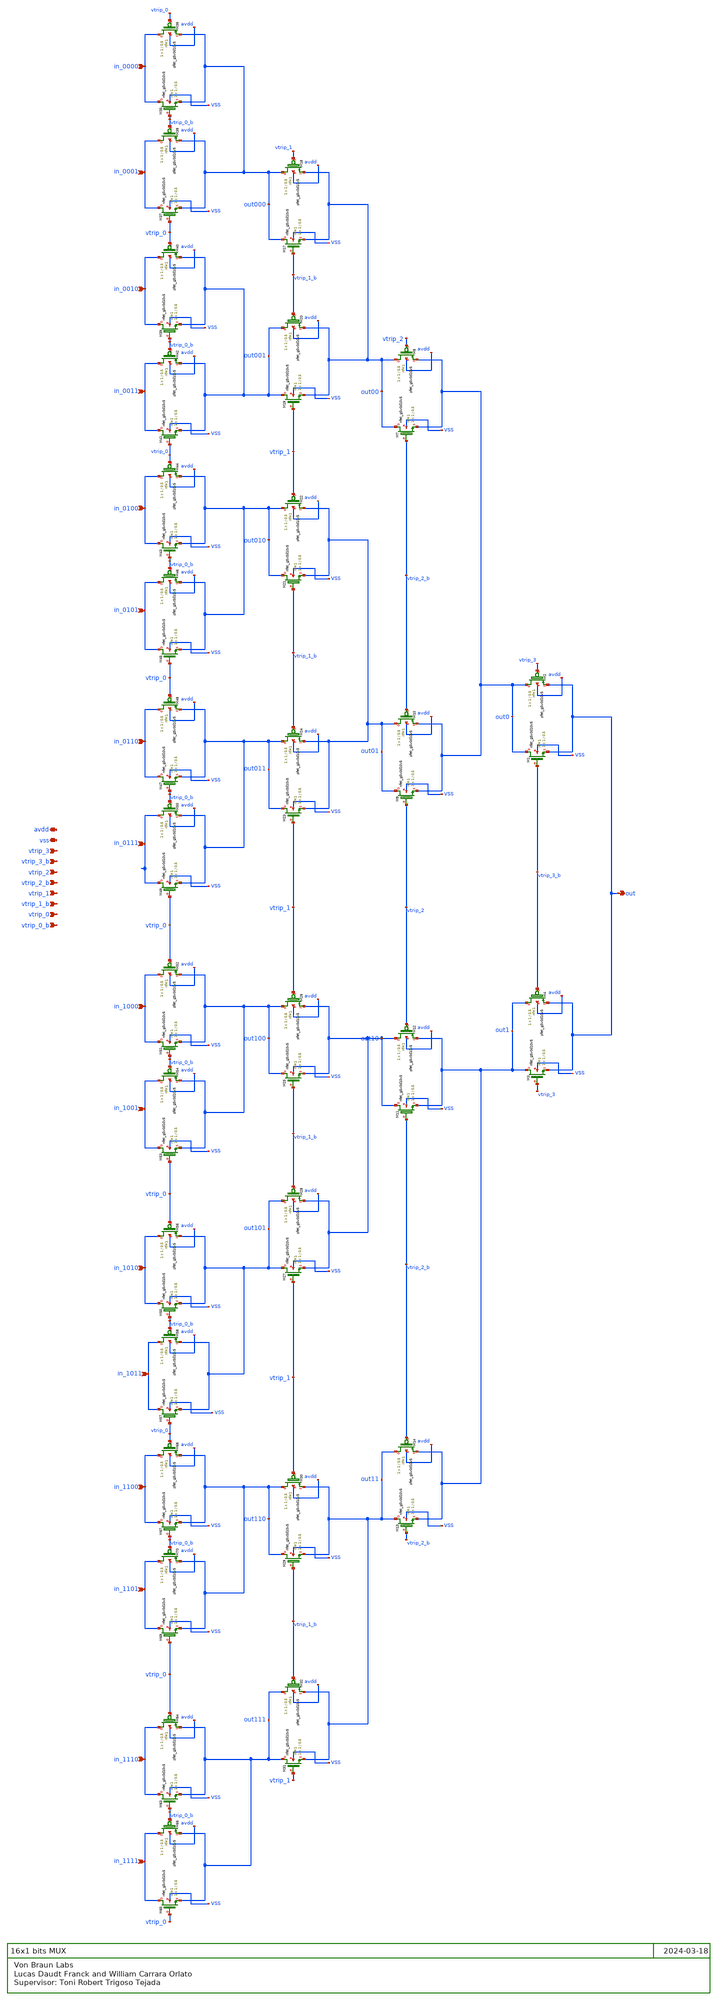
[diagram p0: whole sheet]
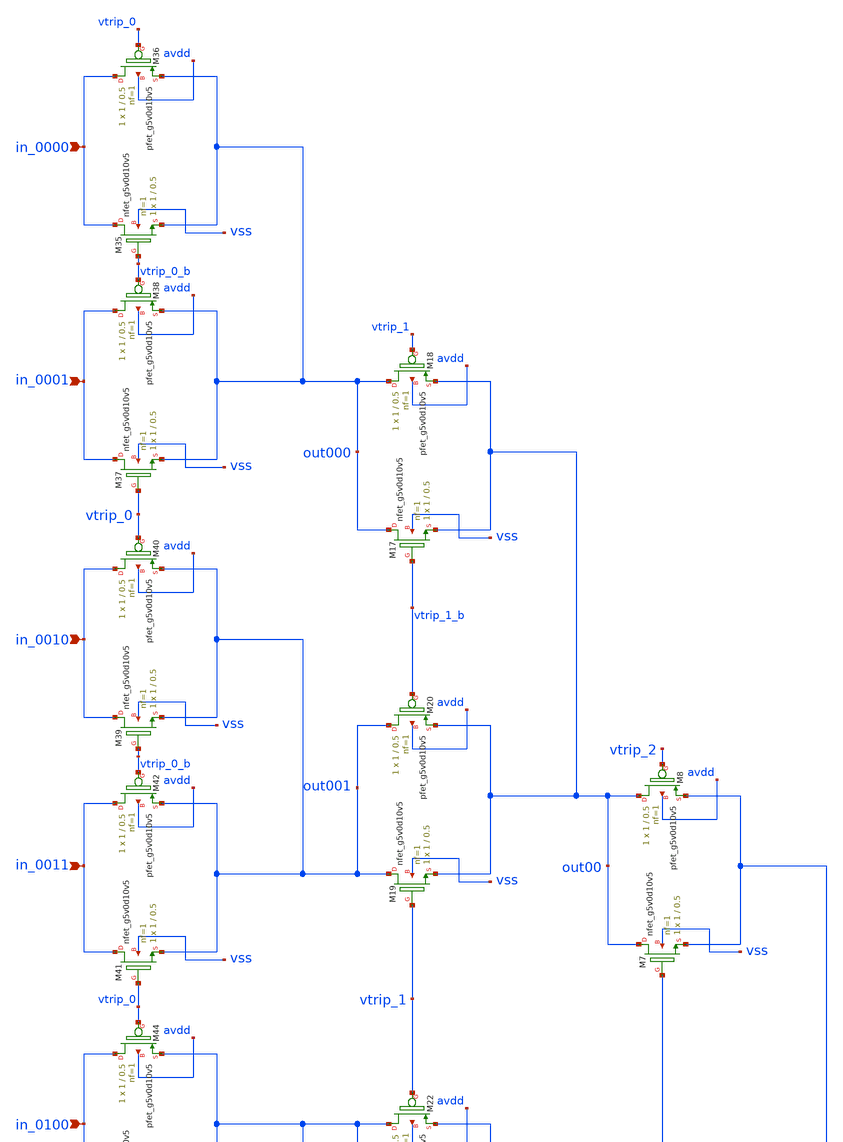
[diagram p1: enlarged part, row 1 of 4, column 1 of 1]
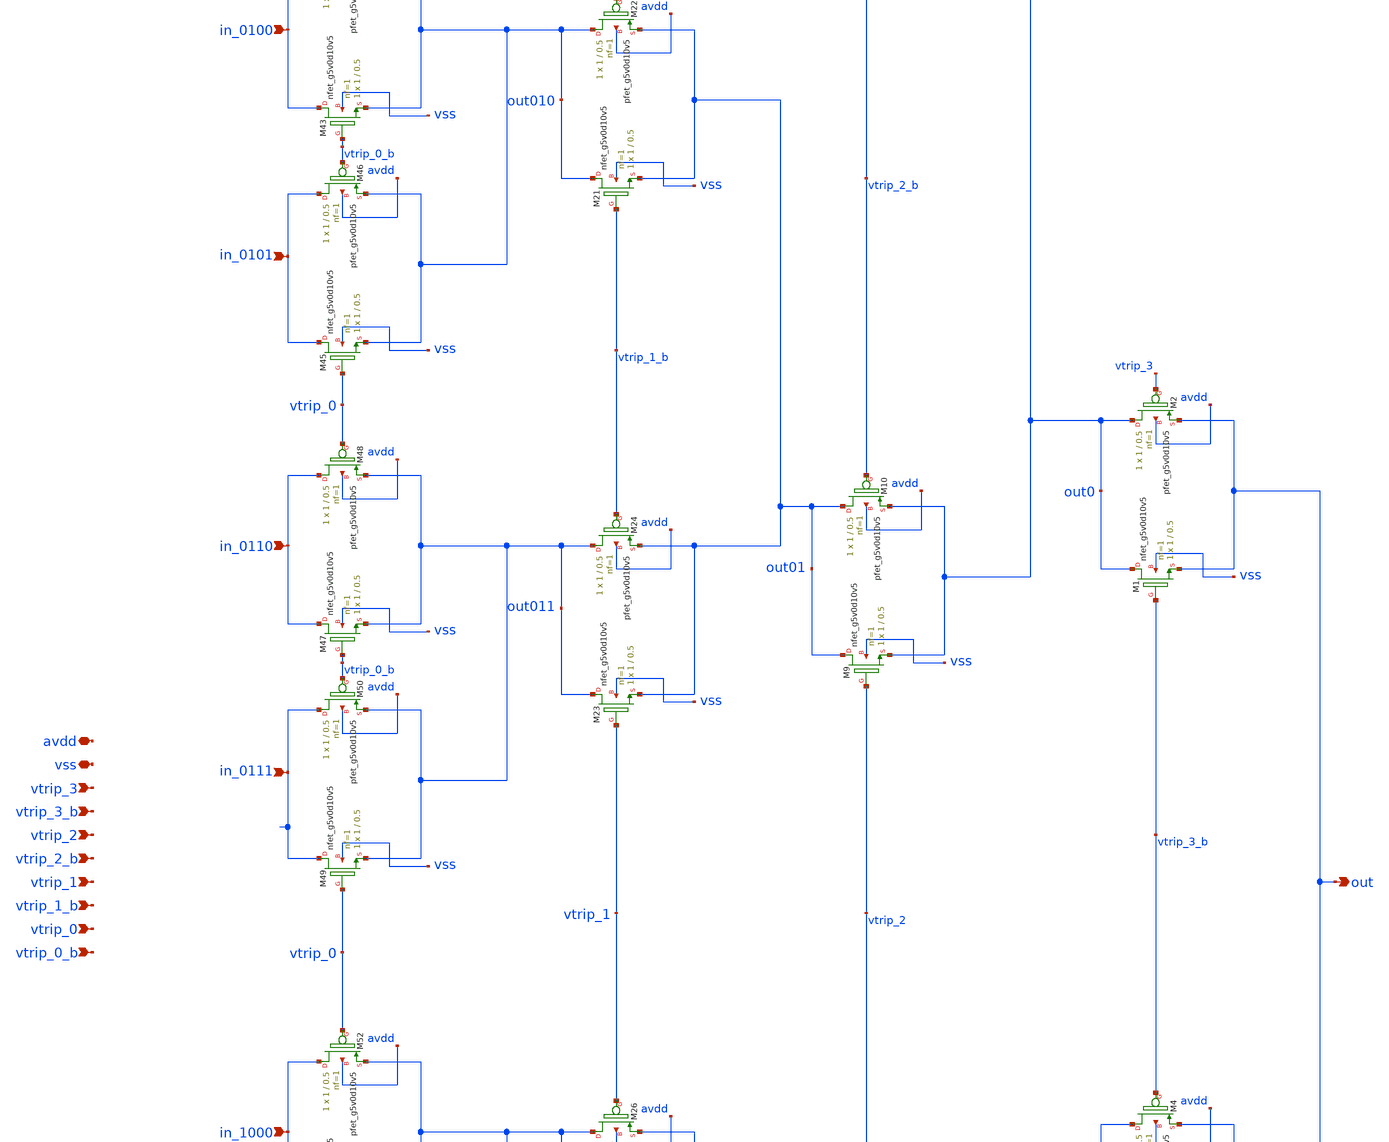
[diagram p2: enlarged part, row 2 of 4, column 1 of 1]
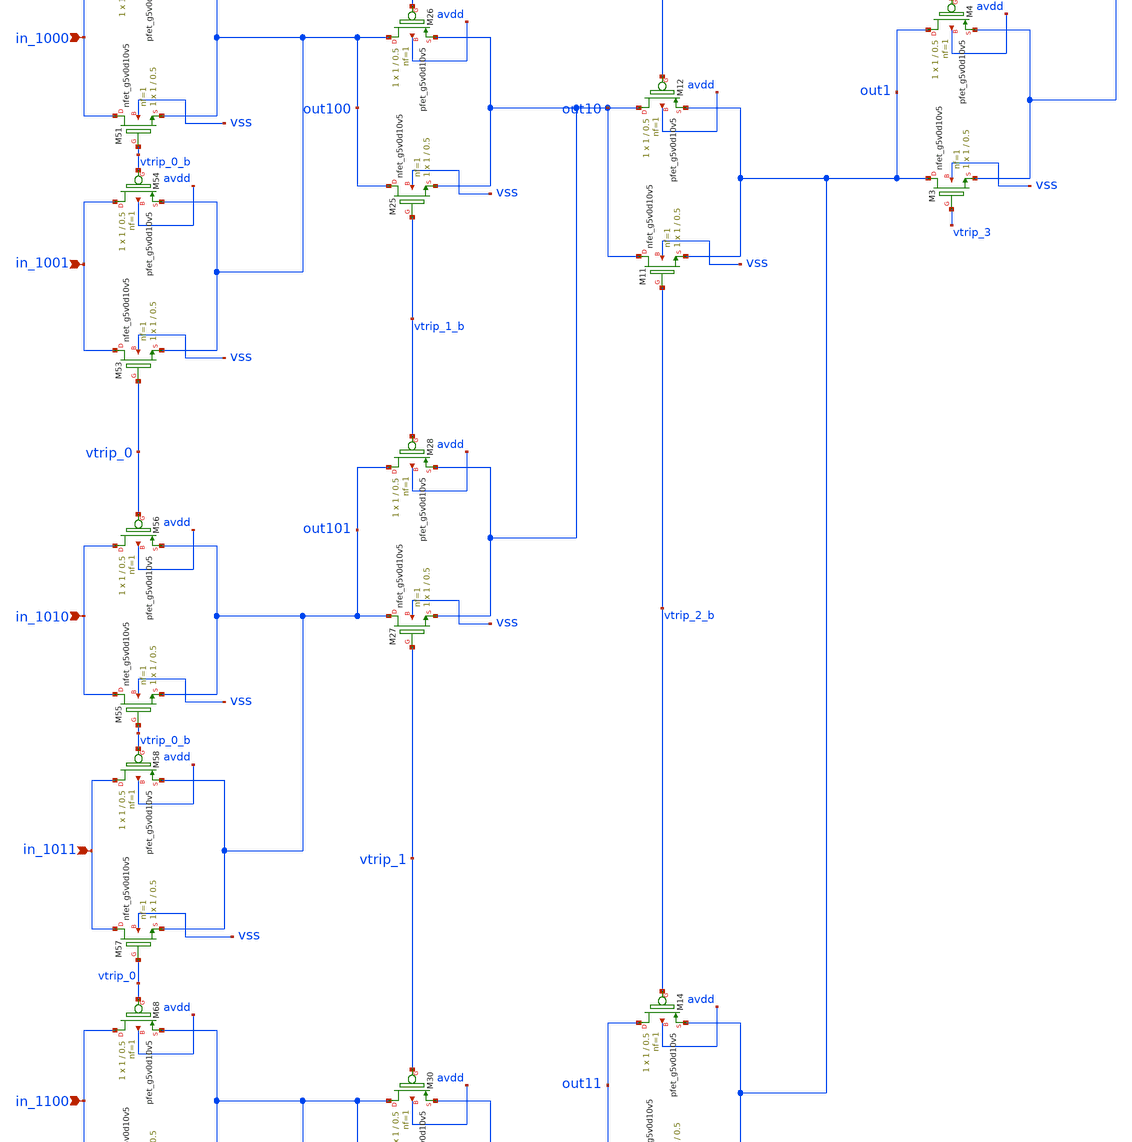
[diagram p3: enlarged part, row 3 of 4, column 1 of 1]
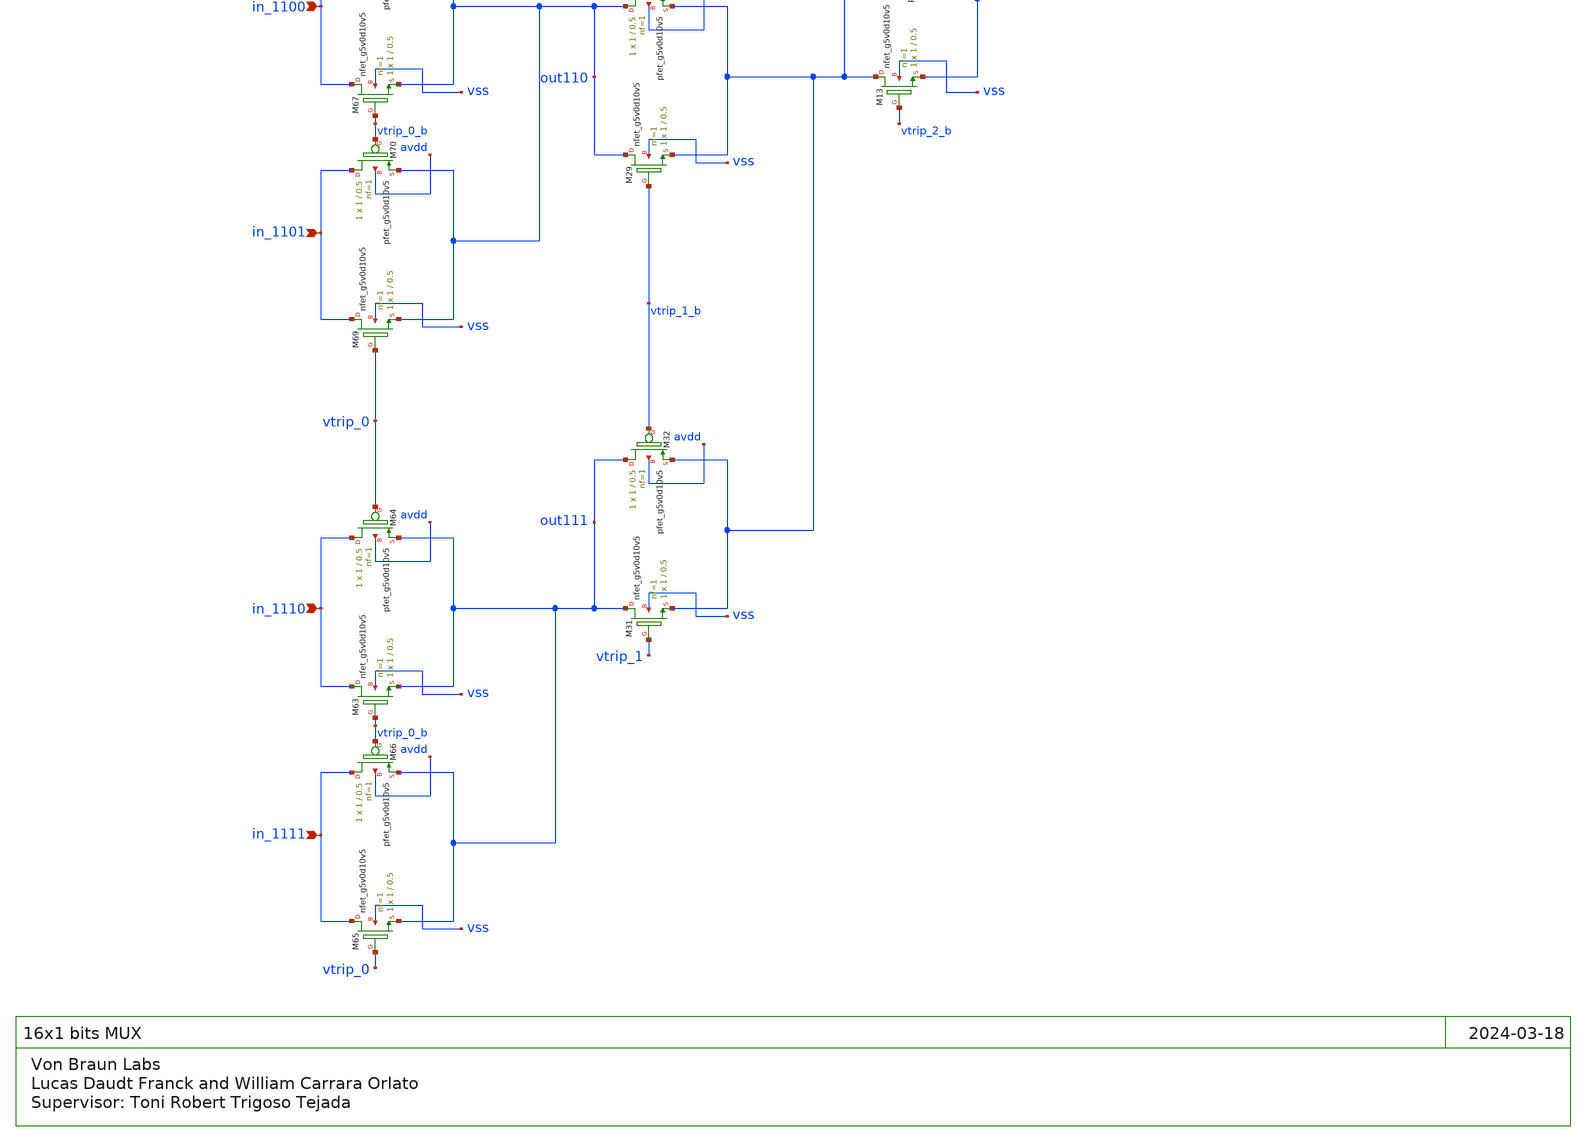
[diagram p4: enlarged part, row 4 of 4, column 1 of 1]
** sch_path: xschem_final/DemuxCompleto.sch
**.subckt DemuxCompleto in_0000 in_0001 in_0010 in_0011 in_0100 in_0101 in_0110 in_0111 in_1000
*+ in_1001 in_1010 in_1011 in_1110 in_1111 in_1100 in_1101 out vtrip_3 vtrip_3_b vtrip_2 vtrip_2_b vtrip_1
*+ vtrip_1_b vtrip_0 vtrip_0_b avdd vss
*.ipin in_0000
*.ipin in_0001
*.ipin in_0010
*.ipin in_0011
*.ipin in_0100
*.ipin in_0101
*.ipin in_0110
*.ipin in_0111
*.ipin in_1000
*.ipin in_1001
*.ipin in_1010
*.ipin in_1011
*.ipin in_1110
*.ipin in_1111
*.ipin in_1100
*.ipin in_1101
*.opin out
*.ipin vtrip_3
*.ipin vtrip_3_b
*.ipin vtrip_2
*.ipin vtrip_2_b
*.ipin vtrip_1
*.ipin vtrip_1_b
*.ipin vtrip_0
*.ipin vtrip_0_b
*.iopin avdd
*.iopin vss
XM1 out0 vtrip_3_b out vss sky130_fd_pr__nfet_g5v0d10v5 L=0.5 W=1 nf=1 ad='int((nf+1)/2) * W/nf * 0.29'
+ as='int((nf+2)/2) * W/nf * 0.29' pd='2*int((nf+1)/2) * (W/nf + 0.29)' ps='2*int((nf+2)/2) * (W/nf + 0.29)'
+ nrd='0.29 / W' nrs='0.29 / W' sa=0 sb=0 sd=0 mult=1 m=1
XM2 out0 vtrip_3 out avdd sky130_fd_pr__pfet_g5v0d10v5 L=0.5 W=1 nf=1 ad='int((nf+1)/2) * W/nf * 0.29'
+ as='int((nf+2)/2) * W/nf * 0.29' pd='2*int((nf+1)/2) * (W/nf + 0.29)' ps='2*int((nf+2)/2) * (W/nf + 0.29)'
+ nrd='0.29 / W' nrs='0.29 / W' sa=0 sb=0 sd=0 mult=1 m=1
XM3 out1 vtrip_3 out vss sky130_fd_pr__nfet_g5v0d10v5 L=0.5 W=1 nf=1 ad='int((nf+1)/2) * W/nf * 0.29'
+ as='int((nf+2)/2) * W/nf * 0.29' pd='2*int((nf+1)/2) * (W/nf + 0.29)' ps='2*int((nf+2)/2) * (W/nf + 0.29)'
+ nrd='0.29 / W' nrs='0.29 / W' sa=0 sb=0 sd=0 mult=1 m=1
XM4 out1 vtrip_3_b out avdd sky130_fd_pr__pfet_g5v0d10v5 L=0.5 W=1 nf=1 ad='int((nf+1)/2) * W/nf * 0.29'
+ as='int((nf+2)/2) * W/nf * 0.29' pd='2*int((nf+1)/2) * (W/nf + 0.29)' ps='2*int((nf+2)/2) * (W/nf + 0.29)'
+ nrd='0.29 / W' nrs='0.29 / W' sa=0 sb=0 sd=0 mult=1 m=1
XM7 out00 vtrip_2_b out0 vss sky130_fd_pr__nfet_g5v0d10v5 L=0.5 W=1 nf=1 ad='int((nf+1)/2) * W/nf * 0.29'
+ as='int((nf+2)/2) * W/nf * 0.29' pd='2*int((nf+1)/2) * (W/nf + 0.29)' ps='2*int((nf+2)/2) * (W/nf + 0.29)'
+ nrd='0.29 / W' nrs='0.29 / W' sa=0 sb=0 sd=0 mult=1 m=1
XM8 out00 vtrip_2 out0 avdd sky130_fd_pr__pfet_g5v0d10v5 L=0.5 W=1 nf=1 ad='int((nf+1)/2) * W/nf * 0.29'
+ as='int((nf+2)/2) * W/nf * 0.29' pd='2*int((nf+1)/2) * (W/nf + 0.29)' ps='2*int((nf+2)/2) * (W/nf + 0.29)'
+ nrd='0.29 / W' nrs='0.29 / W' sa=0 sb=0 sd=0 mult=1 m=1
XM9 out01 vtrip_2 out0 vss sky130_fd_pr__nfet_g5v0d10v5 L=0.5 W=1 nf=1 ad='int((nf+1)/2) * W/nf * 0.29'
+ as='int((nf+2)/2) * W/nf * 0.29' pd='2*int((nf+1)/2) * (W/nf + 0.29)' ps='2*int((nf+2)/2) * (W/nf + 0.29)'
+ nrd='0.29 / W' nrs='0.29 / W' sa=0 sb=0 sd=0 mult=1 m=1
XM10 out01 vtrip_2_b out0 avdd sky130_fd_pr__pfet_g5v0d10v5 L=0.5 W=1 nf=1 ad='int((nf+1)/2) * W/nf * 0.29'
+ as='int((nf+2)/2) * W/nf * 0.29' pd='2*int((nf+1)/2) * (W/nf + 0.29)' ps='2*int((nf+2)/2) * (W/nf + 0.29)'
+ nrd='0.29 / W' nrs='0.29 / W' sa=0 sb=0 sd=0 mult=1 m=1
XM11 out10 vtrip_2_b out1 vss sky130_fd_pr__nfet_g5v0d10v5 L=0.5 W=1 nf=1 ad='int((nf+1)/2) * W/nf * 0.29'
+ as='int((nf+2)/2) * W/nf * 0.29' pd='2*int((nf+1)/2) * (W/nf + 0.29)' ps='2*int((nf+2)/2) * (W/nf + 0.29)'
+ nrd='0.29 / W' nrs='0.29 / W' sa=0 sb=0 sd=0 mult=1 m=1
XM12 out10 vtrip_2 out1 avdd sky130_fd_pr__pfet_g5v0d10v5 L=0.5 W=1 nf=1 ad='int((nf+1)/2) * W/nf * 0.29'
+ as='int((nf+2)/2) * W/nf * 0.29' pd='2*int((nf+1)/2) * (W/nf + 0.29)' ps='2*int((nf+2)/2) * (W/nf + 0.29)'
+ nrd='0.29 / W' nrs='0.29 / W' sa=0 sb=0 sd=0 mult=1 m=1
XM13 out11 vtrip_2_b out1 vss sky130_fd_pr__nfet_g5v0d10v5 L=0.5 W=1 nf=1 ad='int((nf+1)/2) * W/nf * 0.29'
+ as='int((nf+2)/2) * W/nf * 0.29' pd='2*int((nf+1)/2) * (W/nf + 0.29)' ps='2*int((nf+2)/2) * (W/nf + 0.29)'
+ nrd='0.29 / W' nrs='0.29 / W' sa=0 sb=0 sd=0 mult=1 m=1
XM14 out11 vtrip_2_b out1 avdd sky130_fd_pr__pfet_g5v0d10v5 L=0.5 W=1 nf=1 ad='int((nf+1)/2) * W/nf * 0.29'
+ as='int((nf+2)/2) * W/nf * 0.29' pd='2*int((nf+1)/2) * (W/nf + 0.29)' ps='2*int((nf+2)/2) * (W/nf + 0.29)'
+ nrd='0.29 / W' nrs='0.29 / W' sa=0 sb=0 sd=0 mult=1 m=1
XM17 out000 vtrip_1_b out00 vss sky130_fd_pr__nfet_g5v0d10v5 L=0.5 W=1 nf=1 ad='int((nf+1)/2) * W/nf * 0.29'
+ as='int((nf+2)/2) * W/nf * 0.29' pd='2*int((nf+1)/2) * (W/nf + 0.29)' ps='2*int((nf+2)/2) * (W/nf + 0.29)'
+ nrd='0.29 / W' nrs='0.29 / W' sa=0 sb=0 sd=0 mult=1 m=1
XM18 out000 vtrip_1 out00 avdd sky130_fd_pr__pfet_g5v0d10v5 L=0.5 W=1 nf=1 ad='int((nf+1)/2) * W/nf * 0.29'
+ as='int((nf+2)/2) * W/nf * 0.29' pd='2*int((nf+1)/2) * (W/nf + 0.29)' ps='2*int((nf+2)/2) * (W/nf + 0.29)'
+ nrd='0.29 / W' nrs='0.29 / W' sa=0 sb=0 sd=0 mult=1 m=1
XM19 out001 vtrip_1 out00 vss sky130_fd_pr__nfet_g5v0d10v5 L=0.5 W=1 nf=1 ad='int((nf+1)/2) * W/nf * 0.29'
+ as='int((nf+2)/2) * W/nf * 0.29' pd='2*int((nf+1)/2) * (W/nf + 0.29)' ps='2*int((nf+2)/2) * (W/nf + 0.29)'
+ nrd='0.29 / W' nrs='0.29 / W' sa=0 sb=0 sd=0 mult=1 m=1
XM20 out001 vtrip_1_b out00 avdd sky130_fd_pr__pfet_g5v0d10v5 L=0.5 W=1 nf=1 ad='int((nf+1)/2) * W/nf * 0.29'
+ as='int((nf+2)/2) * W/nf * 0.29' pd='2*int((nf+1)/2) * (W/nf + 0.29)' ps='2*int((nf+2)/2) * (W/nf + 0.29)'
+ nrd='0.29 / W' nrs='0.29 / W' sa=0 sb=0 sd=0 mult=1 m=1
XM21 out010 vtrip_1_b out01 vss sky130_fd_pr__nfet_g5v0d10v5 L=0.5 W=1 nf=1 ad='int((nf+1)/2) * W/nf * 0.29'
+ as='int((nf+2)/2) * W/nf * 0.29' pd='2*int((nf+1)/2) * (W/nf + 0.29)' ps='2*int((nf+2)/2) * (W/nf + 0.29)'
+ nrd='0.29 / W' nrs='0.29 / W' sa=0 sb=0 sd=0 mult=1 m=1
XM22 out010 vtrip_1 out01 avdd sky130_fd_pr__pfet_g5v0d10v5 L=0.5 W=1 nf=1 ad='int((nf+1)/2) * W/nf * 0.29'
+ as='int((nf+2)/2) * W/nf * 0.29' pd='2*int((nf+1)/2) * (W/nf + 0.29)' ps='2*int((nf+2)/2) * (W/nf + 0.29)'
+ nrd='0.29 / W' nrs='0.29 / W' sa=0 sb=0 sd=0 mult=1 m=1
XM23 out011 vtrip_1 out01 vss sky130_fd_pr__nfet_g5v0d10v5 L=0.5 W=1 nf=1 ad='int((nf+1)/2) * W/nf * 0.29'
+ as='int((nf+2)/2) * W/nf * 0.29' pd='2*int((nf+1)/2) * (W/nf + 0.29)' ps='2*int((nf+2)/2) * (W/nf + 0.29)'
+ nrd='0.29 / W' nrs='0.29 / W' sa=0 sb=0 sd=0 mult=1 m=1
XM24 out011 vtrip_1_b out01 avdd sky130_fd_pr__pfet_g5v0d10v5 L=0.5 W=1 nf=1 ad='int((nf+1)/2) * W/nf * 0.29'
+ as='int((nf+2)/2) * W/nf * 0.29' pd='2*int((nf+1)/2) * (W/nf + 0.29)' ps='2*int((nf+2)/2) * (W/nf + 0.29)'
+ nrd='0.29 / W' nrs='0.29 / W' sa=0 sb=0 sd=0 mult=1 m=1
XM25 out100 vtrip_1_b out10 vss sky130_fd_pr__nfet_g5v0d10v5 L=0.5 W=1 nf=1 ad='int((nf+1)/2) * W/nf * 0.29'
+ as='int((nf+2)/2) * W/nf * 0.29' pd='2*int((nf+1)/2) * (W/nf + 0.29)' ps='2*int((nf+2)/2) * (W/nf + 0.29)'
+ nrd='0.29 / W' nrs='0.29 / W' sa=0 sb=0 sd=0 mult=1 m=1
XM26 out100 vtrip_1 out10 avdd sky130_fd_pr__pfet_g5v0d10v5 L=0.5 W=1 nf=1 ad='int((nf+1)/2) * W/nf * 0.29'
+ as='int((nf+2)/2) * W/nf * 0.29' pd='2*int((nf+1)/2) * (W/nf + 0.29)' ps='2*int((nf+2)/2) * (W/nf + 0.29)'
+ nrd='0.29 / W' nrs='0.29 / W' sa=0 sb=0 sd=0 mult=1 m=1
XM27 out101 vtrip_1 out10 vss sky130_fd_pr__nfet_g5v0d10v5 L=0.5 W=1 nf=1 ad='int((nf+1)/2) * W/nf * 0.29'
+ as='int((nf+2)/2) * W/nf * 0.29' pd='2*int((nf+1)/2) * (W/nf + 0.29)' ps='2*int((nf+2)/2) * (W/nf + 0.29)'
+ nrd='0.29 / W' nrs='0.29 / W' sa=0 sb=0 sd=0 mult=1 m=1
XM28 out101 vtrip_1_b out10 avdd sky130_fd_pr__pfet_g5v0d10v5 L=0.5 W=1 nf=1 ad='int((nf+1)/2) * W/nf * 0.29'
+ as='int((nf+2)/2) * W/nf * 0.29' pd='2*int((nf+1)/2) * (W/nf + 0.29)' ps='2*int((nf+2)/2) * (W/nf + 0.29)'
+ nrd='0.29 / W' nrs='0.29 / W' sa=0 sb=0 sd=0 mult=1 m=1
XM29 out110 vtrip_1_b out11 vss sky130_fd_pr__nfet_g5v0d10v5 L=0.5 W=1 nf=1 ad='int((nf+1)/2) * W/nf * 0.29'
+ as='int((nf+2)/2) * W/nf * 0.29' pd='2*int((nf+1)/2) * (W/nf + 0.29)' ps='2*int((nf+2)/2) * (W/nf + 0.29)'
+ nrd='0.29 / W' nrs='0.29 / W' sa=0 sb=0 sd=0 mult=1 m=1
XM30 out110 vtrip_1 out11 avdd sky130_fd_pr__pfet_g5v0d10v5 L=0.5 W=1 nf=1 ad='int((nf+1)/2) * W/nf * 0.29'
+ as='int((nf+2)/2) * W/nf * 0.29' pd='2*int((nf+1)/2) * (W/nf + 0.29)' ps='2*int((nf+2)/2) * (W/nf + 0.29)'
+ nrd='0.29 / W' nrs='0.29 / W' sa=0 sb=0 sd=0 mult=1 m=1
XM31 out111 vtrip_1 out11 vss sky130_fd_pr__nfet_g5v0d10v5 L=0.5 W=1 nf=1 ad='int((nf+1)/2) * W/nf * 0.29'
+ as='int((nf+2)/2) * W/nf * 0.29' pd='2*int((nf+1)/2) * (W/nf + 0.29)' ps='2*int((nf+2)/2) * (W/nf + 0.29)'
+ nrd='0.29 / W' nrs='0.29 / W' sa=0 sb=0 sd=0 mult=1 m=1
XM32 out111 vtrip_1_b out11 avdd sky130_fd_pr__pfet_g5v0d10v5 L=0.5 W=1 nf=1 ad='int((nf+1)/2) * W/nf * 0.29'
+ as='int((nf+2)/2) * W/nf * 0.29' pd='2*int((nf+1)/2) * (W/nf + 0.29)' ps='2*int((nf+2)/2) * (W/nf + 0.29)'
+ nrd='0.29 / W' nrs='0.29 / W' sa=0 sb=0 sd=0 mult=1 m=1
XM35 in_0000 vtrip_0_b out000 vss sky130_fd_pr__nfet_g5v0d10v5 L=0.5 W=1 nf=1 ad='int((nf+1)/2) * W/nf * 0.29'
+ as='int((nf+2)/2) * W/nf * 0.29' pd='2*int((nf+1)/2) * (W/nf + 0.29)' ps='2*int((nf+2)/2) * (W/nf + 0.29)'
+ nrd='0.29 / W' nrs='0.29 / W' sa=0 sb=0 sd=0 mult=1 m=1
XM36 in_0000 vtrip_0 out000 avdd sky130_fd_pr__pfet_g5v0d10v5 L=0.5 W=1 nf=1 ad='int((nf+1)/2) * W/nf * 0.29'
+ as='int((nf+2)/2) * W/nf * 0.29' pd='2*int((nf+1)/2) * (W/nf + 0.29)' ps='2*int((nf+2)/2) * (W/nf + 0.29)'
+ nrd='0.29 / W' nrs='0.29 / W' sa=0 sb=0 sd=0 mult=1 m=1
XM37 in_0001 vtrip_0 out000 vss sky130_fd_pr__nfet_g5v0d10v5 L=0.5 W=1 nf=1 ad='int((nf+1)/2) * W/nf * 0.29'
+ as='int((nf+2)/2) * W/nf * 0.29' pd='2*int((nf+1)/2) * (W/nf + 0.29)' ps='2*int((nf+2)/2) * (W/nf + 0.29)'
+ nrd='0.29 / W' nrs='0.29 / W' sa=0 sb=0 sd=0 mult=1 m=1
XM38 in_0001 vtrip_0_b out000 avdd sky130_fd_pr__pfet_g5v0d10v5 L=0.5 W=1 nf=1 ad='int((nf+1)/2) * W/nf * 0.29'
+ as='int((nf+2)/2) * W/nf * 0.29' pd='2*int((nf+1)/2) * (W/nf + 0.29)' ps='2*int((nf+2)/2) * (W/nf + 0.29)'
+ nrd='0.29 / W' nrs='0.29 / W' sa=0 sb=0 sd=0 mult=1 m=1
XM39 in_0010 vtrip_0_b out001 vss sky130_fd_pr__nfet_g5v0d10v5 L=0.5 W=1 nf=1 ad='int((nf+1)/2) * W/nf * 0.29'
+ as='int((nf+2)/2) * W/nf * 0.29' pd='2*int((nf+1)/2) * (W/nf + 0.29)' ps='2*int((nf+2)/2) * (W/nf + 0.29)'
+ nrd='0.29 / W' nrs='0.29 / W' sa=0 sb=0 sd=0 mult=1 m=1
XM40 in_0010 vtrip_0 out001 avdd sky130_fd_pr__pfet_g5v0d10v5 L=0.5 W=1 nf=1 ad='int((nf+1)/2) * W/nf * 0.29'
+ as='int((nf+2)/2) * W/nf * 0.29' pd='2*int((nf+1)/2) * (W/nf + 0.29)' ps='2*int((nf+2)/2) * (W/nf + 0.29)'
+ nrd='0.29 / W' nrs='0.29 / W' sa=0 sb=0 sd=0 mult=1 m=1
XM41 in_0011 vtrip_0 out001 vss sky130_fd_pr__nfet_g5v0d10v5 L=0.5 W=1 nf=1 ad='int((nf+1)/2) * W/nf * 0.29'
+ as='int((nf+2)/2) * W/nf * 0.29' pd='2*int((nf+1)/2) * (W/nf + 0.29)' ps='2*int((nf+2)/2) * (W/nf + 0.29)'
+ nrd='0.29 / W' nrs='0.29 / W' sa=0 sb=0 sd=0 mult=1 m=1
XM42 in_0011 vtrip_0_b out001 avdd sky130_fd_pr__pfet_g5v0d10v5 L=0.5 W=1 nf=1 ad='int((nf+1)/2) * W/nf * 0.29'
+ as='int((nf+2)/2) * W/nf * 0.29' pd='2*int((nf+1)/2) * (W/nf + 0.29)' ps='2*int((nf+2)/2) * (W/nf + 0.29)'
+ nrd='0.29 / W' nrs='0.29 / W' sa=0 sb=0 sd=0 mult=1 m=1
XM43 in_0100 vtrip_0_b out010 vss sky130_fd_pr__nfet_g5v0d10v5 L=0.5 W=1 nf=1 ad='int((nf+1)/2) * W/nf * 0.29'
+ as='int((nf+2)/2) * W/nf * 0.29' pd='2*int((nf+1)/2) * (W/nf + 0.29)' ps='2*int((nf+2)/2) * (W/nf + 0.29)'
+ nrd='0.29 / W' nrs='0.29 / W' sa=0 sb=0 sd=0 mult=1 m=1
XM44 in_0100 vtrip_0 out010 avdd sky130_fd_pr__pfet_g5v0d10v5 L=0.5 W=1 nf=1 ad='int((nf+1)/2) * W/nf * 0.29'
+ as='int((nf+2)/2) * W/nf * 0.29' pd='2*int((nf+1)/2) * (W/nf + 0.29)' ps='2*int((nf+2)/2) * (W/nf + 0.29)'
+ nrd='0.29 / W' nrs='0.29 / W' sa=0 sb=0 sd=0 mult=1 m=1
XM45 in_0101 vtrip_0 out010 vss sky130_fd_pr__nfet_g5v0d10v5 L=0.5 W=1 nf=1 ad='int((nf+1)/2) * W/nf * 0.29'
+ as='int((nf+2)/2) * W/nf * 0.29' pd='2*int((nf+1)/2) * (W/nf + 0.29)' ps='2*int((nf+2)/2) * (W/nf + 0.29)'
+ nrd='0.29 / W' nrs='0.29 / W' sa=0 sb=0 sd=0 mult=1 m=1
XM46 in_0101 vtrip_0_b out010 avdd sky130_fd_pr__pfet_g5v0d10v5 L=0.5 W=1 nf=1 ad='int((nf+1)/2) * W/nf * 0.29'
+ as='int((nf+2)/2) * W/nf * 0.29' pd='2*int((nf+1)/2) * (W/nf + 0.29)' ps='2*int((nf+2)/2) * (W/nf + 0.29)'
+ nrd='0.29 / W' nrs='0.29 / W' sa=0 sb=0 sd=0 mult=1 m=1
XM47 in_0110 vtrip_0_b out011 vss sky130_fd_pr__nfet_g5v0d10v5 L=0.5 W=1 nf=1 ad='int((nf+1)/2) * W/nf * 0.29'
+ as='int((nf+2)/2) * W/nf * 0.29' pd='2*int((nf+1)/2) * (W/nf + 0.29)' ps='2*int((nf+2)/2) * (W/nf + 0.29)'
+ nrd='0.29 / W' nrs='0.29 / W' sa=0 sb=0 sd=0 mult=1 m=1
XM48 in_0110 vtrip_0 out011 avdd sky130_fd_pr__pfet_g5v0d10v5 L=0.5 W=1 nf=1 ad='int((nf+1)/2) * W/nf * 0.29'
+ as='int((nf+2)/2) * W/nf * 0.29' pd='2*int((nf+1)/2) * (W/nf + 0.29)' ps='2*int((nf+2)/2) * (W/nf + 0.29)'
+ nrd='0.29 / W' nrs='0.29 / W' sa=0 sb=0 sd=0 mult=1 m=1
XM49 in_0111 vtrip_0 out011 vss sky130_fd_pr__nfet_g5v0d10v5 L=0.5 W=1 nf=1 ad='int((nf+1)/2) * W/nf * 0.29'
+ as='int((nf+2)/2) * W/nf * 0.29' pd='2*int((nf+1)/2) * (W/nf + 0.29)' ps='2*int((nf+2)/2) * (W/nf + 0.29)'
+ nrd='0.29 / W' nrs='0.29 / W' sa=0 sb=0 sd=0 mult=1 m=1
XM50 in_0111 vtrip_0_b out011 avdd sky130_fd_pr__pfet_g5v0d10v5 L=0.5 W=1 nf=1 ad='int((nf+1)/2) * W/nf * 0.29'
+ as='int((nf+2)/2) * W/nf * 0.29' pd='2*int((nf+1)/2) * (W/nf + 0.29)' ps='2*int((nf+2)/2) * (W/nf + 0.29)'
+ nrd='0.29 / W' nrs='0.29 / W' sa=0 sb=0 sd=0 mult=1 m=1
XM51 in_1000 vtrip_0_b out100 vss sky130_fd_pr__nfet_g5v0d10v5 L=0.5 W=1 nf=1 ad='int((nf+1)/2) * W/nf * 0.29'
+ as='int((nf+2)/2) * W/nf * 0.29' pd='2*int((nf+1)/2) * (W/nf + 0.29)' ps='2*int((nf+2)/2) * (W/nf + 0.29)'
+ nrd='0.29 / W' nrs='0.29 / W' sa=0 sb=0 sd=0 mult=1 m=1
XM52 in_1000 vtrip_0 out100 avdd sky130_fd_pr__pfet_g5v0d10v5 L=0.5 W=1 nf=1 ad='int((nf+1)/2) * W/nf * 0.29'
+ as='int((nf+2)/2) * W/nf * 0.29' pd='2*int((nf+1)/2) * (W/nf + 0.29)' ps='2*int((nf+2)/2) * (W/nf + 0.29)'
+ nrd='0.29 / W' nrs='0.29 / W' sa=0 sb=0 sd=0 mult=1 m=1
XM53 in_1001 vtrip_0 out100 vss sky130_fd_pr__nfet_g5v0d10v5 L=0.5 W=1 nf=1 ad='int((nf+1)/2) * W/nf * 0.29'
+ as='int((nf+2)/2) * W/nf * 0.29' pd='2*int((nf+1)/2) * (W/nf + 0.29)' ps='2*int((nf+2)/2) * (W/nf + 0.29)'
+ nrd='0.29 / W' nrs='0.29 / W' sa=0 sb=0 sd=0 mult=1 m=1
XM54 in_1001 vtrip_0_b out100 avdd sky130_fd_pr__pfet_g5v0d10v5 L=0.5 W=1 nf=1 ad='int((nf+1)/2) * W/nf * 0.29'
+ as='int((nf+2)/2) * W/nf * 0.29' pd='2*int((nf+1)/2) * (W/nf + 0.29)' ps='2*int((nf+2)/2) * (W/nf + 0.29)'
+ nrd='0.29 / W' nrs='0.29 / W' sa=0 sb=0 sd=0 mult=1 m=1
XM55 in_1010 vtrip_0_b out101 vss sky130_fd_pr__nfet_g5v0d10v5 L=0.5 W=1 nf=1 ad='int((nf+1)/2) * W/nf * 0.29'
+ as='int((nf+2)/2) * W/nf * 0.29' pd='2*int((nf+1)/2) * (W/nf + 0.29)' ps='2*int((nf+2)/2) * (W/nf + 0.29)'
+ nrd='0.29 / W' nrs='0.29 / W' sa=0 sb=0 sd=0 mult=1 m=1
XM56 in_1010 vtrip_0 out101 avdd sky130_fd_pr__pfet_g5v0d10v5 L=0.5 W=1 nf=1 ad='int((nf+1)/2) * W/nf * 0.29'
+ as='int((nf+2)/2) * W/nf * 0.29' pd='2*int((nf+1)/2) * (W/nf + 0.29)' ps='2*int((nf+2)/2) * (W/nf + 0.29)'
+ nrd='0.29 / W' nrs='0.29 / W' sa=0 sb=0 sd=0 mult=1 m=1
XM57 in_1011 vtrip_0 out101 vss sky130_fd_pr__nfet_g5v0d10v5 L=0.5 W=1 nf=1 ad='int((nf+1)/2) * W/nf * 0.29'
+ as='int((nf+2)/2) * W/nf * 0.29' pd='2*int((nf+1)/2) * (W/nf + 0.29)' ps='2*int((nf+2)/2) * (W/nf + 0.29)'
+ nrd='0.29 / W' nrs='0.29 / W' sa=0 sb=0 sd=0 mult=1 m=1
XM58 in_1011 vtrip_0_b out101 avdd sky130_fd_pr__pfet_g5v0d10v5 L=0.5 W=1 nf=1 ad='int((nf+1)/2) * W/nf * 0.29'
+ as='int((nf+2)/2) * W/nf * 0.29' pd='2*int((nf+1)/2) * (W/nf + 0.29)' ps='2*int((nf+2)/2) * (W/nf + 0.29)'
+ nrd='0.29 / W' nrs='0.29 / W' sa=0 sb=0 sd=0 mult=1 m=1
XM63 in_1110 vtrip_0_b out111 vss sky130_fd_pr__nfet_g5v0d10v5 L=0.5 W=1 nf=1 ad='int((nf+1)/2) * W/nf * 0.29'
+ as='int((nf+2)/2) * W/nf * 0.29' pd='2*int((nf+1)/2) * (W/nf + 0.29)' ps='2*int((nf+2)/2) * (W/nf + 0.29)'
+ nrd='0.29 / W' nrs='0.29 / W' sa=0 sb=0 sd=0 mult=1 m=1
XM64 in_1110 vtrip_0 out111 avdd sky130_fd_pr__pfet_g5v0d10v5 L=0.5 W=1 nf=1 ad='int((nf+1)/2) * W/nf * 0.29'
+ as='int((nf+2)/2) * W/nf * 0.29' pd='2*int((nf+1)/2) * (W/nf + 0.29)' ps='2*int((nf+2)/2) * (W/nf + 0.29)'
+ nrd='0.29 / W' nrs='0.29 / W' sa=0 sb=0 sd=0 mult=1 m=1
XM65 in_1111 vtrip_0 out111 vss sky130_fd_pr__nfet_g5v0d10v5 L=0.5 W=1 nf=1 ad='int((nf+1)/2) * W/nf * 0.29'
+ as='int((nf+2)/2) * W/nf * 0.29' pd='2*int((nf+1)/2) * (W/nf + 0.29)' ps='2*int((nf+2)/2) * (W/nf + 0.29)'
+ nrd='0.29 / W' nrs='0.29 / W' sa=0 sb=0 sd=0 mult=1 m=1
XM66 in_1111 vtrip_0_b out111 avdd sky130_fd_pr__pfet_g5v0d10v5 L=0.5 W=1 nf=1 ad='int((nf+1)/2) * W/nf * 0.29'
+ as='int((nf+2)/2) * W/nf * 0.29' pd='2*int((nf+1)/2) * (W/nf + 0.29)' ps='2*int((nf+2)/2) * (W/nf + 0.29)'
+ nrd='0.29 / W' nrs='0.29 / W' sa=0 sb=0 sd=0 mult=1 m=1
XM67 in_1100 vtrip_0_b out110 vss sky130_fd_pr__nfet_g5v0d10v5 L=0.5 W=1 nf=1 ad='int((nf+1)/2) * W/nf * 0.29'
+ as='int((nf+2)/2) * W/nf * 0.29' pd='2*int((nf+1)/2) * (W/nf + 0.29)' ps='2*int((nf+2)/2) * (W/nf + 0.29)'
+ nrd='0.29 / W' nrs='0.29 / W' sa=0 sb=0 sd=0 mult=1 m=1
XM68 in_1100 vtrip_0 out110 avdd sky130_fd_pr__pfet_g5v0d10v5 L=0.5 W=1 nf=1 ad='int((nf+1)/2) * W/nf * 0.29'
+ as='int((nf+2)/2) * W/nf * 0.29' pd='2*int((nf+1)/2) * (W/nf + 0.29)' ps='2*int((nf+2)/2) * (W/nf + 0.29)'
+ nrd='0.29 / W' nrs='0.29 / W' sa=0 sb=0 sd=0 mult=1 m=1
XM69 in_1101 vtrip_0 out110 vss sky130_fd_pr__nfet_g5v0d10v5 L=0.5 W=1 nf=1 ad='int((nf+1)/2) * W/nf * 0.29'
+ as='int((nf+2)/2) * W/nf * 0.29' pd='2*int((nf+1)/2) * (W/nf + 0.29)' ps='2*int((nf+2)/2) * (W/nf + 0.29)'
+ nrd='0.29 / W' nrs='0.29 / W' sa=0 sb=0 sd=0 mult=1 m=1
XM70 in_1101 vtrip_0_b out110 avdd sky130_fd_pr__pfet_g5v0d10v5 L=0.5 W=1 nf=1 ad='int((nf+1)/2) * W/nf * 0.29'
+ as='int((nf+2)/2) * W/nf * 0.29' pd='2*int((nf+1)/2) * (W/nf + 0.29)' ps='2*int((nf+2)/2) * (W/nf + 0.29)'
+ nrd='0.29 / W' nrs='0.29 / W' sa=0 sb=0 sd=0 mult=1 m=1
**.ends
.end
